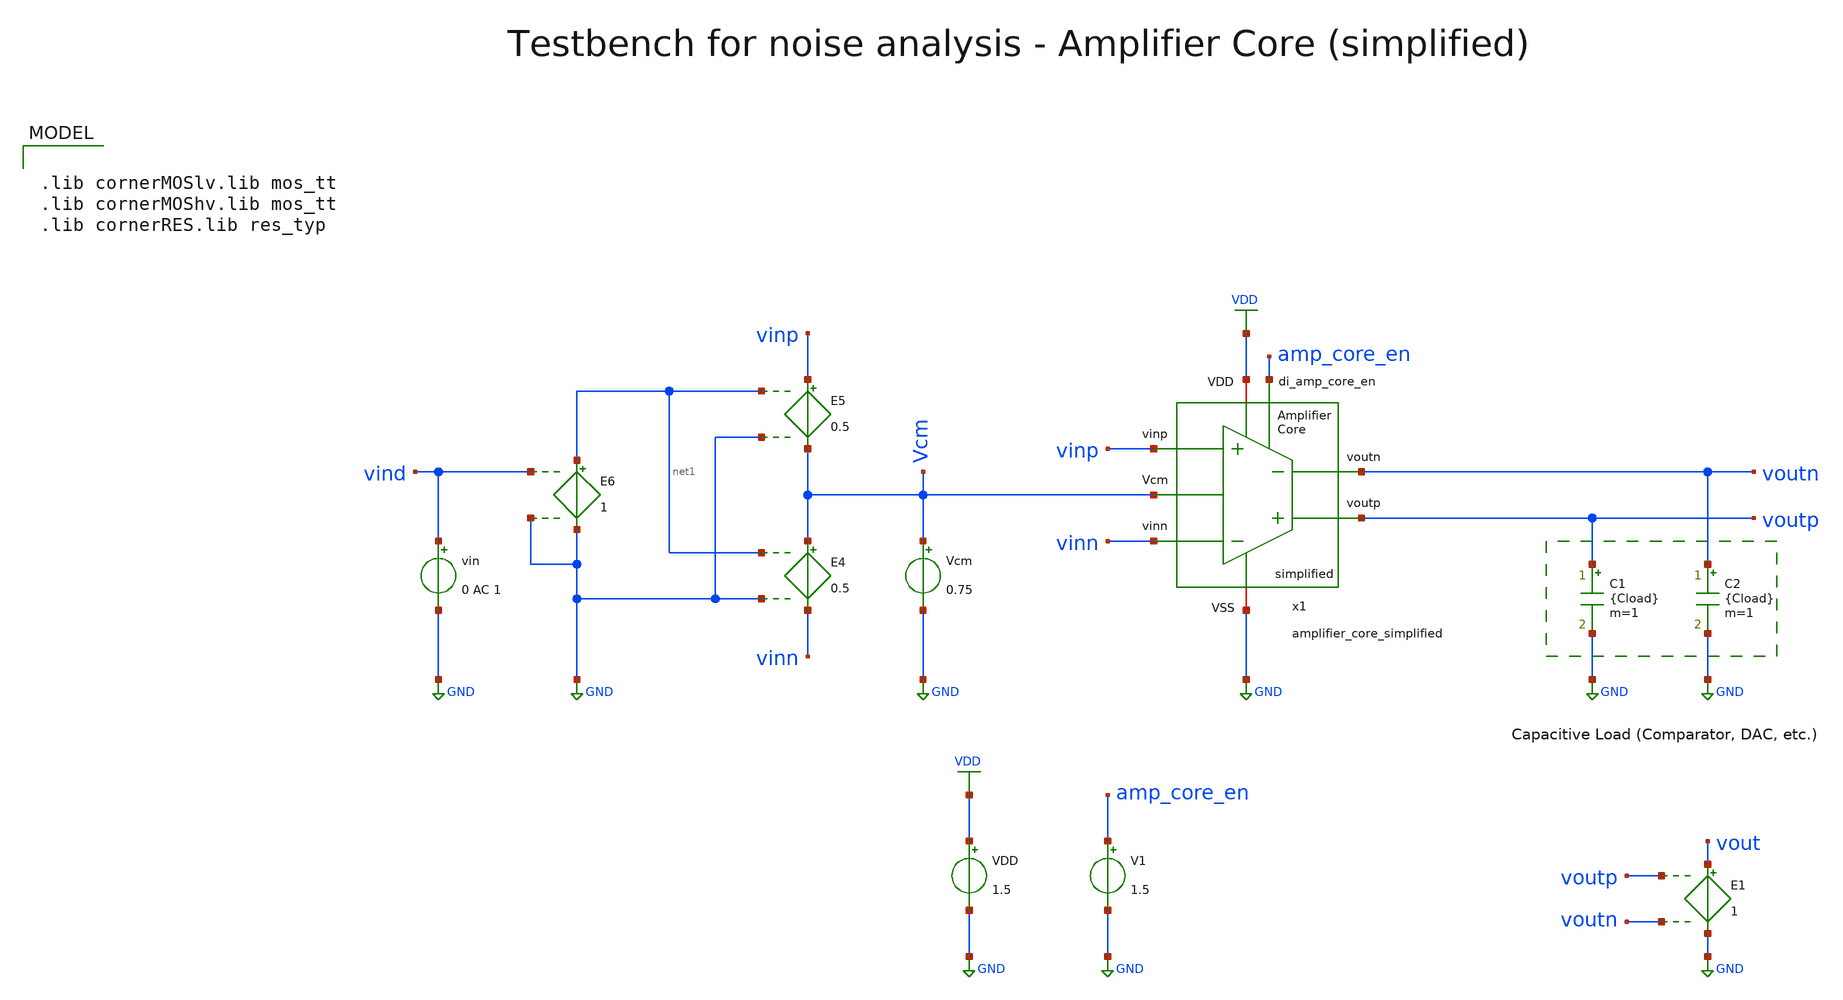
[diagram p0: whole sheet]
** sch_path: SG13G2_ATBS-ADC-main/xschem/bio_amplifier/amplifier_core/testbenches/amplifier_core_simplified_tb_noise.sch
**.subckt amplifier_core_simplified_tb_noise
VDD VDD GND 1.5
C1 voutp GND {Cload} m=1
C2 voutn GND {Cload} m=1
Vcm Vcm GND 0.75
E4 Vcm vinn net1 GND 0.5
E5 vinp Vcm net1 GND 0.5
E6 net1 GND vind GND 1
V1 amp_core_en GND 1.5
E1 vout GND voutp voutn 1
vin vind GND 0 AC 1
x1 voutp voutn amp_core_en vinn vinp VDD GND Vcm amplifier_core_simplified
**** begin user architecture code

.lib cornerMOSlv.lib mos_tt
.lib cornerMOShv.lib mos_tt
.lib cornerRES.lib res_typ



.param temp=27
* 228fF DAC + (1 - beta) * 3.3pF
.param Cload=3.49p
.options savecurrents method=gear reltol=1e-2 abstol=1e-15 gmin=1e-15
.control

optran 0 0 0 1u 1m 0

save all

set wr_vecnames
set wr_singlescale
set enable_noisy_r

* User Constants
let f_min = 0.15
let f_max = 500
* let f_min = 10m
* let f_max = 1G

* Operating Point Analysis
op
remzerovec
write amplifier_core_simplified_tb_noise.raw
set appendwrite

* Noise Analysis
noise v(vout) vin dec 101 $&const.f_min $&const.f_max 1

* Plotting
setplot noise1
plot inoise_spectrum ylog xlog ylabel 'Input Noise'
plot onoise_spectrum ylog xlog ylabel 'Output Noise'
write amplifier_core_simplified_tb_noise.raw
set appendwrite

* Write Data
set wr_vecnames
set wr_singlescale
wrdata
+ /foss/designs/SG13G2_ATBS-ADC-main/python/plot_simulations/data/amplifier_core_simplified_tb_noise.txt v(inoise_spectrum) v(onoise_spectrum)

* Measurements
setplot noise2
print inoise_total
print onoise_total


*quit
.endc


**** end user architecture code
**.ends
.GLOBAL GND
.GLOBAL VDD
.end
